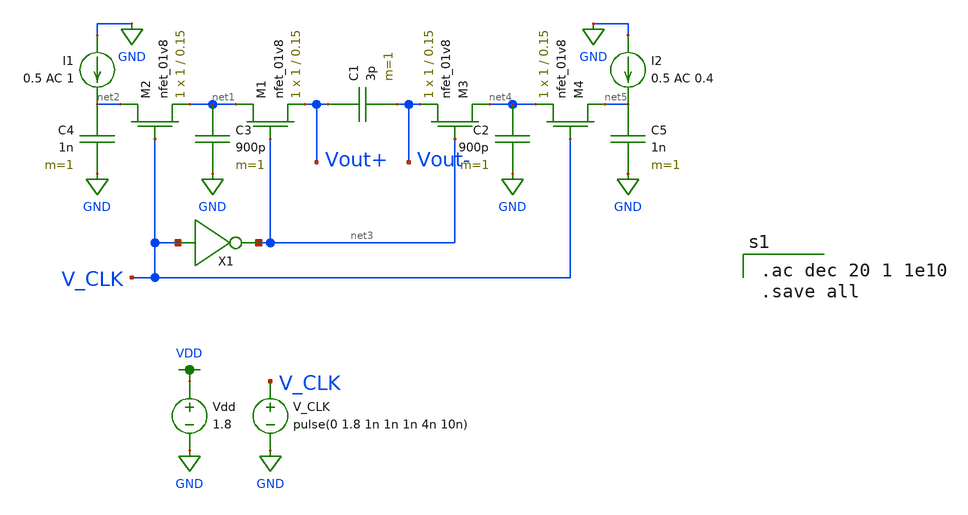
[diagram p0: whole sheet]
** sch_path: simulation/archived/filter_switch_cap_tran.sch
**.subckt filter_switch_cap_tran
Vdd VDD GND 1.8
V_CLK V_CLK GND pulse(0 1.8 1n 1n 1n 4n 10n)
C1 Vout+ Vout- 3p m=1
I1 GND net2 0.5 AC 1
C3 net1 GND 900p m=1
XM1 net1 net3 Vout+ GND sky130_fd_pr__nfet_01v8 L=0.15 W=1 nf=1 ad='int((nf+1)/2) * W/nf * 0.29' as='int((nf+2)/2) * W/nf * 0.29'
+ pd='2*int((nf+1)/2) * (W/nf + 0.29)' ps='2*int((nf+2)/2) * (W/nf + 0.29)' nrd='0.29 / W' nrs='0.29 / W'
+ sa=0 sb=0 sd=0 mult=1 m=1
XM2 net2 V_CLK net1 GND sky130_fd_pr__nfet_01v8 L=0.15 W=1 nf=1 ad='int((nf+1)/2) * W/nf * 0.29' as='int((nf+2)/2) * W/nf * 0.29'
+ pd='2*int((nf+1)/2) * (W/nf + 0.29)' ps='2*int((nf+2)/2) * (W/nf + 0.29)' nrd='0.29 / W' nrs='0.29 / W'
+ sa=0 sb=0 sd=0 mult=1 m=1
C4 net2 GND 1n m=1
X1 V_CLK net3 inverter
I2 GND net5 0.5 AC 0.4
C2 net4 GND 900p m=1
XM3 net4 net3 Vout- GND sky130_fd_pr__nfet_01v8 L=0.15 W=1 nf=1 ad='int((nf+1)/2) * W/nf * 0.29' as='int((nf+2)/2) * W/nf * 0.29'
+ pd='2*int((nf+1)/2) * (W/nf + 0.29)' ps='2*int((nf+2)/2) * (W/nf + 0.29)' nrd='0.29 / W' nrs='0.29 / W'
+ sa=0 sb=0 sd=0 mult=1 m=1
XM4 net5 V_CLK net4 GND sky130_fd_pr__nfet_01v8 L=0.15 W=1 nf=1 ad='int((nf+1)/2) * W/nf * 0.29' as='int((nf+2)/2) * W/nf * 0.29'
+ pd='2*int((nf+1)/2) * (W/nf + 0.29)' ps='2*int((nf+2)/2) * (W/nf + 0.29)' nrd='0.29 / W' nrs='0.29 / W'
+ sa=0 sb=0 sd=0 mult=1 m=1
C5 net5 GND 1n m=1
**** begin user architecture code

.ac dec 20 1 1e10
.save all


.option wnflag=1
.param MC_SWITCH=0.0
.lib ~/skywater/skywater-pdk/libraries/sky130_fd_pr_ngspice/latest/models/sky130.lib.spice tt

**** end user architecture code
**.ends

* expanding   symbol:  /home/madvlsi/VLSI_Sine_Gen/simulation/dac/inverter.sym # of pins=2
** sym_path: simulation/dac/inverter.sym
** sch_path: simulation/dac/inverter.sch
.subckt inverter A Y
*.ipin A
*.opin Y
XM1 Y A VDD VDD sky130_fd_pr__pfet_01v8 L=0.15 W=1 nf=1 ad='int((nf+1)/2) * W/nf * 0.29' as='int((nf+2)/2) * W/nf * 0.29'
+ pd='2*int((nf+1)/2) * (W/nf + 0.29)' ps='2*int((nf+2)/2) * (W/nf + 0.29)' nrd='0.29 / W' nrs='0.29 / W'
+ sa=0 sb=0 sd=0 mult=1 m=1
XM2 Y A GND GND sky130_fd_pr__nfet_01v8 L=0.15 W=1 nf=1 ad='int((nf+1)/2) * W/nf * 0.29' as='int((nf+2)/2) * W/nf * 0.29'
+ pd='2*int((nf+1)/2) * (W/nf + 0.29)' ps='2*int((nf+2)/2) * (W/nf + 0.29)' nrd='0.29 / W' nrs='0.29 / W'
+ sa=0 sb=0 sd=0 mult=1 m=1
.ends

.GLOBAL GND
.GLOBAL VDD
.end
